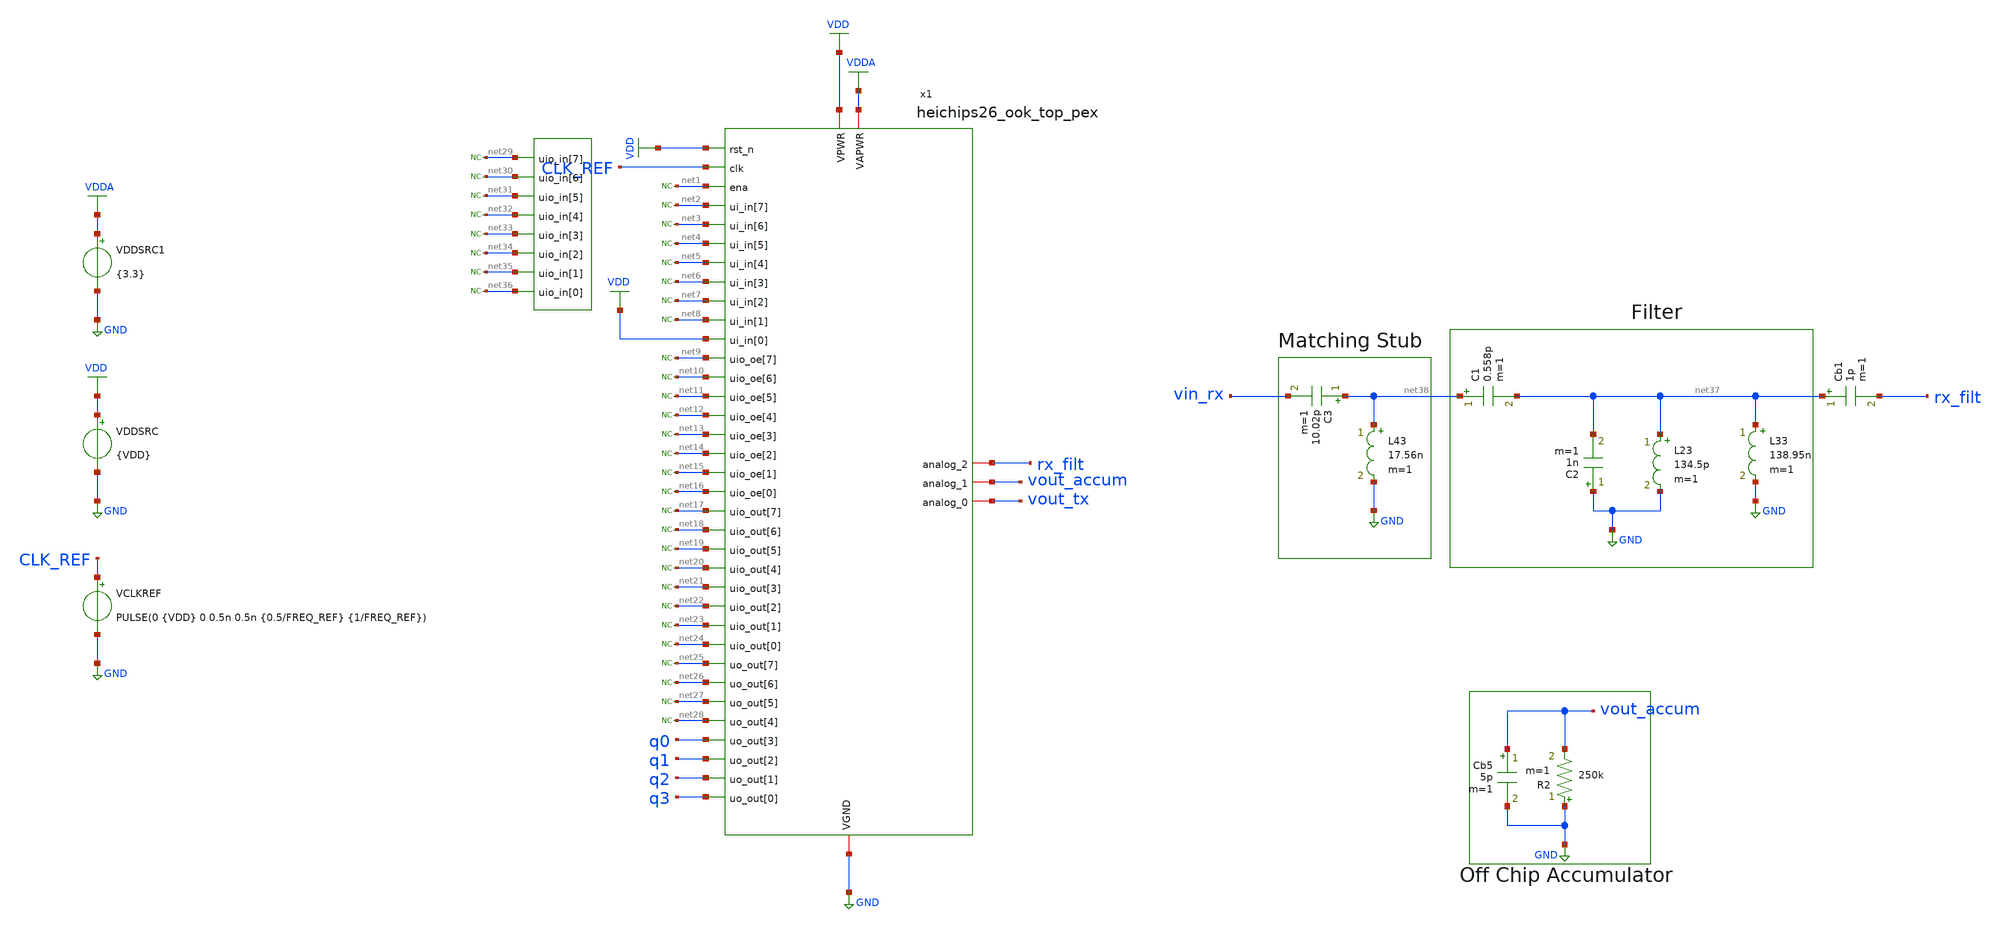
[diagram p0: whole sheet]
** sch_path: macros/heichips26_ook_top/testbenches/xschem/heichipts26_ook_top_tb_tran.sch
**.subckt heichipts26_ook_top_tb_tran
VCLKREF CLK_REF GND PULSE(0 {VDD} 0 0.5n 0.5n {0.5/FREQ_REF} {1/FREQ_REF})
VDDSRC VDD GND {VDD}
VDDSRC1 VDDA GND {3.3}
Cb5 vout_accum GND 5p m=1
R2 GND vout_accum 250k m=1
x1 net1 net19 net9 net2 net10 net20 net3 net21 net11 net22 net12 net4 net5 net13 net23 net24 net14
+ net6 VDD VDDA net7 net15 net25 rx_filt vout_accum vout_tx q0 q1 q2 q3 net8 net26 net16 VDD CLK_REF VDD
+ net27 net17 GND net18 net28 net29 net30 net31 net32 net33 net34 net35 net36 heichips26_ook_top_pex
* noconn #net28
* noconn #net27
* noconn #net26
* noconn #net25
* noconn #net24
* noconn #net23
* noconn #net22
* noconn #net21
* noconn #net20
* noconn #net19
* noconn #net18
* noconn #net17
* noconn #net16
* noconn #net15
* noconn #net14
* noconn #net13
* noconn #net12
* noconn #net11
* noconn #net10
* noconn #net9
* noconn #net8
* noconn #net7
* noconn #net6
* noconn #net5
* noconn #net4
* noconn #net3
* noconn #net2
* noconn #net1
* noconn #net36
* noconn #net35
* noconn #net34
* noconn #net33
* noconn #net32
* noconn #net31
* noconn #net30
* noconn #net29
Cb1 net37 rx_filt 1p m=1
C2 GND net37 1n m=1
L23 net37 GND 134.5p m=1
C1 net38 net37 0.558p m=1
L33 net37 GND 138.95n m=1
C3 net38 vin_rx 10.02p m=1
L43 net38 GND 17.56n m=1
**** begin user architecture code


.param VDD=1.5
.param FREQ_REF=80e6
.param FREQ_FB=600e6
.options klu reltol=1e-3 abstol=1e-12 vntol=1e-6 gmin=1e-6 itl1=200 rshunt=1e9 trtol=20
.param b0=1 b1=0 b2=1 b3=0 b4=0 b5=1 b6=0 b7=1
.param bitsum={b0+b1+b2+b3+b4+b5+b6+b7}
.param parity={bitsum-2*int(bitsum/2)}

Vcarrier ncar 0 SINE(0 1m 433.92e6)

Bvenv nenv 0 V =  (time<10e-6)  ? 1 :  (time<15e-6)  ? (1-b0) : (time<20e-6) ? b0 :  (time<25e-6)  ?
+ (1-b1) : (time<30e-6) ? b1 :  (time<35e-6)  ? (1-b2) : (time<40e-6) ? b2 :  (time<45e-6)  ? (1-b3) :
+ (time<50e-6) ? b3 :  (time<55e-6)  ? (1-b4) : (time<60e-6) ? b4 :  (time<65e-6)  ? (1-b5) : (time<70e-6) ? b5 :
+  (time<75e-6)  ? (1-b6) : (time<80e-6) ? b6 :  (time<85e-6)  ? (1-b7) : (time<90e-6) ? b7 :  (time<100e-6) ?
+ parity :  1

Bvin1 vin_rx_src 0 V={(V(nenv)*V(ncar))}
Rsrc vin_rx_src vin_rx 50
.save vout_tx q0 q1 q2 q3 vout_accum vin_rx rx_filt i(VDDSRC) i(VDDSRC1)
.tran 100p 150u 0 100p uic



.lib cornerMOSlv.lib mos_tt
.lib cornerMOShv.lib mos_tt
.lib cornerRES.lib res_typ
.lib cornerDIO.lib dio_tt
.lib cornerCAP.lib cap_typ
.include /home/belal/HeiChips/heichips26-on-off/macros/heichips26_ook_top/macros/dac/netlist/xspice/dac.xspice
.include /home/belal/HeiChips/heichips26-on-off/macros/heichips26_ook_top/macros/ook_analog_system/netlist/pex/ook_transmitter_magic_pex_3.spice
.include /home/belal/HeiChips/heichips26-on-off/macros/heichips26_ook_top/macros/ook_analog_system/netlist/pex/ook_analog_system_magic_pex_3.spice
.include /home/belal/HeiChips/heichips26-on-off/IHP-Open-PDK/ihp-sg13cmos5l/libs.tech/ngspice/models/cap_mfringe.lib
.include /home/belal/HeiChips/heichips26-on-off/macros/heichips26_ook_top/macros/ook_analog_system/netlist/pex/vco_magic_pex_3.spice
.include /home/belal/HeiChips/heichips26-on-off/macros/heichips26_ook_top/macros/ook_analog_system/netlist/pex/output_buffer_magic_pex_3.spice
.include /home/belal/HeiChips/heichips26-on-off/macros/heichips26_ook_top/netlist/pex/heichips26_ook_top_magic_pex_3.spice


**** end user architecture code
**.ends
.GLOBAL GND
.GLOBAL VDD
.GLOBAL VDDA
.end
